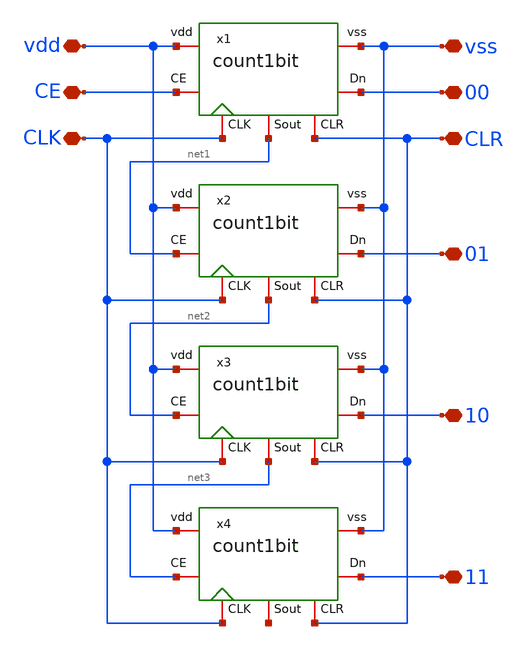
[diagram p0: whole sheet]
** sch_path: design/blocks/count4bits/schematic/count4bits.sch
**.subckt count4bits CE vdd vss CLK 00 01 CLR 10 11
*.iopin CE
*.iopin vdd
*.iopin vss
*.iopin CLK
*.iopin 00
*.iopin 01
*.iopin CLR
*.iopin 10
*.iopin 11
x1 vdd 00 CLK CE vss CLR net1 count1bit
x2 vdd 01 CLK net1 vss CLR net2 count1bit
x3 vdd 10 CLK net2 vss CLR net3 count1bit
x4 vdd 11 CLK net3 vss CLR net4 count1bit
**.ends
.end
